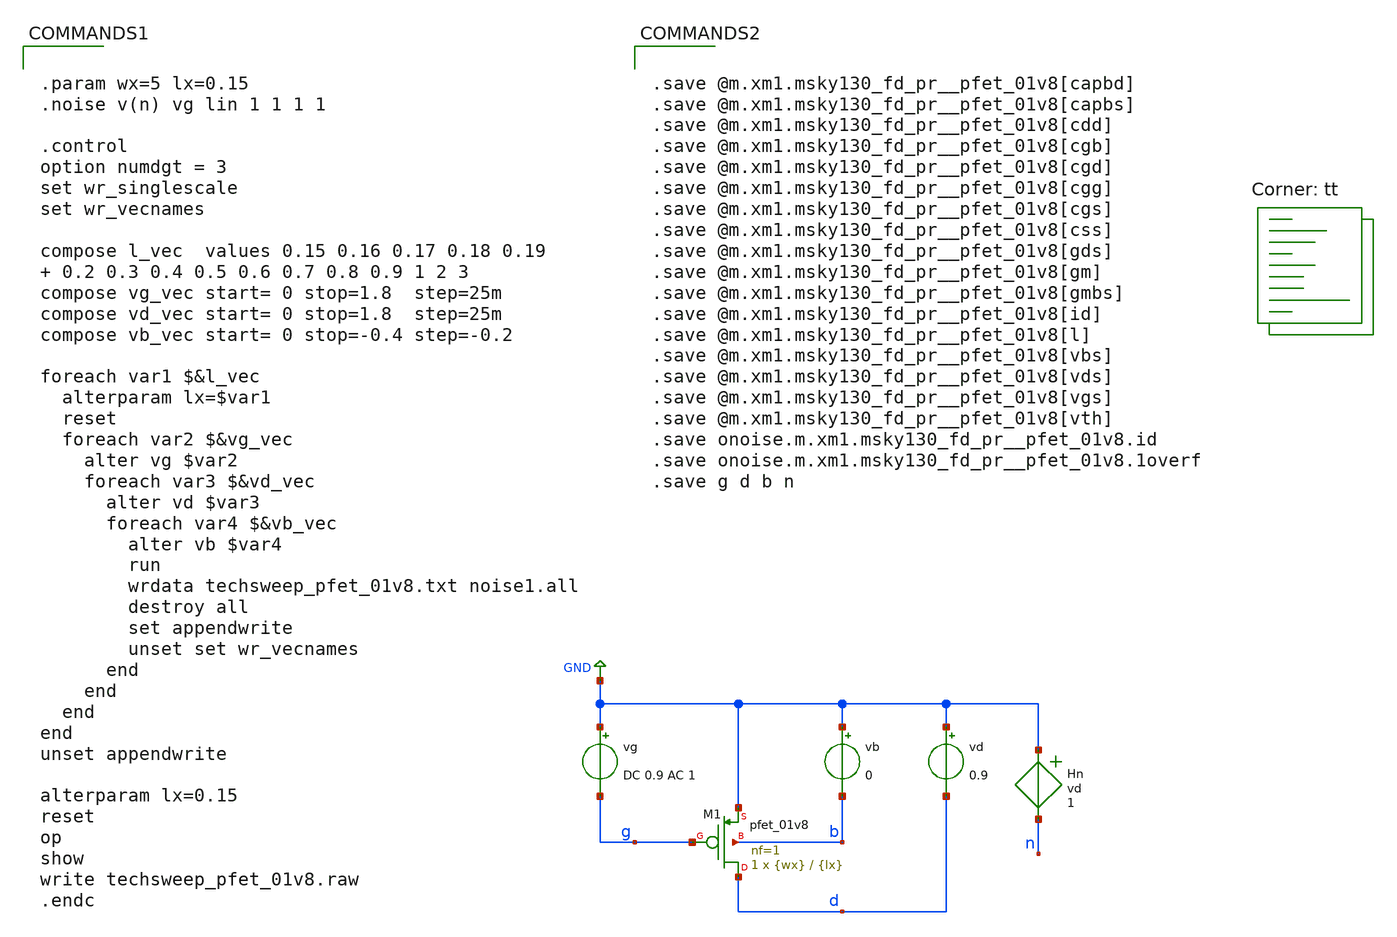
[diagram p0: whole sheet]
** sch_path: ISSCC25/submitted_notebooks/analog_vibes/OTA/scripts/techsweep/techsweep_pfet_01v8.sch
**.subckt techsweep_pfet_01v8
Hn GND n vd 1
vg GND g DC 0.9 AC 1
vd GND d 0.9
vb GND b 0
XM1 d g GND b sky130_fd_pr__pfet_01v8 L={lx} W={wx} nf=1 ad='int((nf+1)/2) * W/nf * 0.29' as='int((nf+2)/2) * W/nf * 0.29'
+ pd='2*int((nf+1)/2) * (W/nf + 0.29)' ps='2*int((nf+2)/2) * (W/nf + 0.29)' nrd='0.29 / W' nrs='0.29 / W'
+ sa=0 sb=0 sd=0 mult=1 m=1
**** begin user architecture code


.param wx=5 lx=0.15
.noise v(n) vg lin 1 1 1 1

.control
option numdgt = 3
set wr_singlescale
set wr_vecnames

compose l_vec  values 0.15 0.16 0.17 0.18 0.19  0.2 0.3 0.4 0.5 0.6 0.7 0.8 0.9 1 2 3
compose vg_vec start= 0 stop=1.8  step=25m
compose vd_vec start= 0 stop=1.8  step=25m
compose vb_vec start= 0 stop=-0.4 step=-0.2

foreach var1 $&l_vec
  alterparam lx=$var1
  reset
  foreach var2 $&vg_vec
    alter vg $var2
    foreach var3 $&vd_vec
      alter vd $var3
      foreach var4 $&vb_vec
        alter vb $var4
        run
        wrdata techsweep_pfet_01v8.txt noise1.all
        destroy all
        set appendwrite
        unset set wr_vecnames
      end
    end
  end
end
unset appendwrite

alterparam lx=0.15
reset
op
show
write techsweep_pfet_01v8.raw
.endc


.lib $::SKYWATER_MODELS/sky130.lib.spice tt


.save @m.xm1.msky130_fd_pr__pfet_01v8[capbd]
.save @m.xm1.msky130_fd_pr__pfet_01v8[capbs]
.save @m.xm1.msky130_fd_pr__pfet_01v8[cdd]
.save @m.xm1.msky130_fd_pr__pfet_01v8[cgb]
.save @m.xm1.msky130_fd_pr__pfet_01v8[cgd]
.save @m.xm1.msky130_fd_pr__pfet_01v8[cgg]
.save @m.xm1.msky130_fd_pr__pfet_01v8[cgs]
.save @m.xm1.msky130_fd_pr__pfet_01v8[css]
.save @m.xm1.msky130_fd_pr__pfet_01v8[gds]
.save @m.xm1.msky130_fd_pr__pfet_01v8[gm]
.save @m.xm1.msky130_fd_pr__pfet_01v8[gmbs]
.save @m.xm1.msky130_fd_pr__pfet_01v8[id]
.save @m.xm1.msky130_fd_pr__pfet_01v8[l]
.save @m.xm1.msky130_fd_pr__pfet_01v8[vbs]
.save @m.xm1.msky130_fd_pr__pfet_01v8[vds]
.save @m.xm1.msky130_fd_pr__pfet_01v8[vgs]
.save @m.xm1.msky130_fd_pr__pfet_01v8[vth]
.save onoise.m.xm1.msky130_fd_pr__pfet_01v8.id
.save onoise.m.xm1.msky130_fd_pr__pfet_01v8.1overf
.save g d b n


**** end user architecture code
**.ends
.GLOBAL GND
.end
